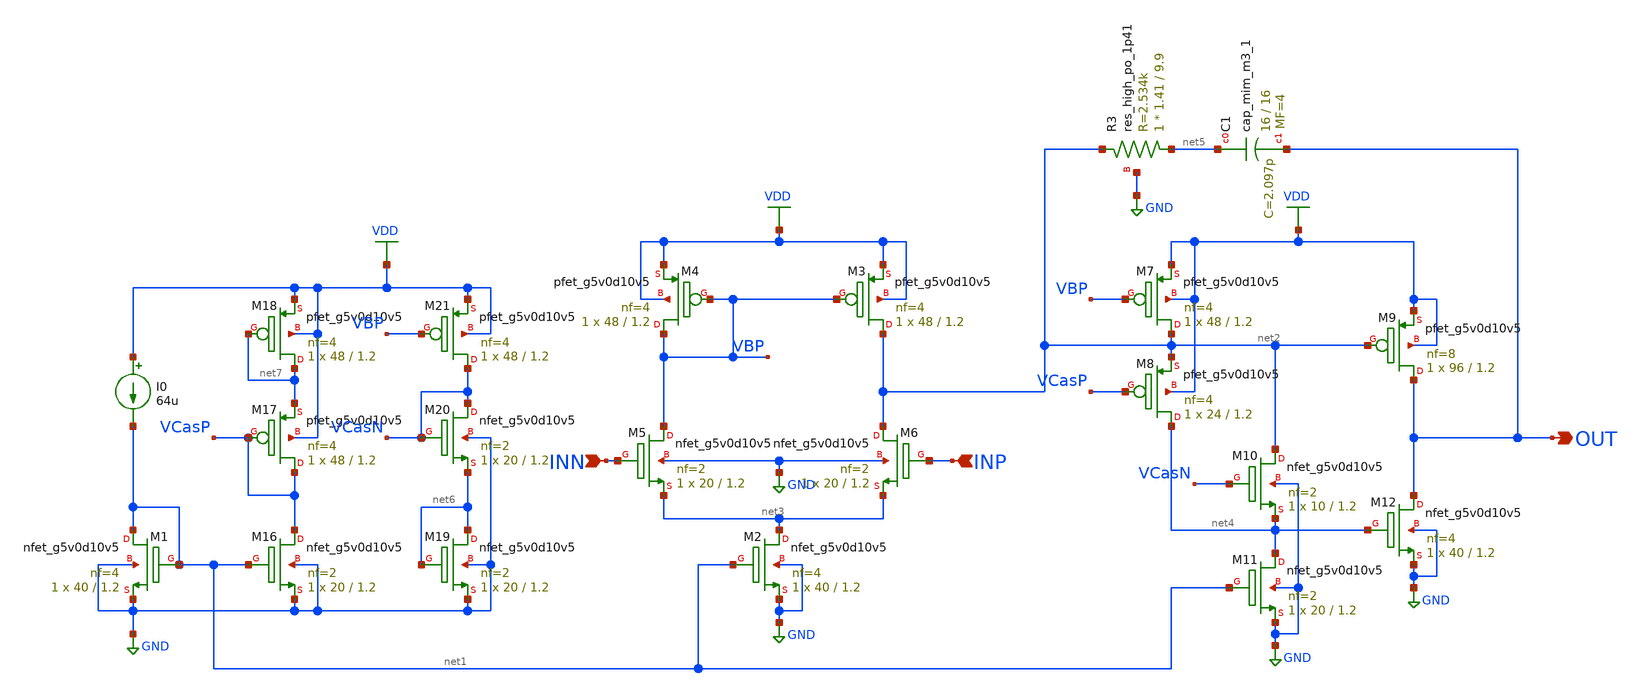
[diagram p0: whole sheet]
** sch_path: Amplifier_PushPull.sch
**.subckt Amplifier_PushPull INN OUT INP
*.ipin INN
*.opin OUT
*.ipin INP
XM1 net1 net1 GND GND sky130_fd_pr__nfet_g5v0d10v5 L=1.2 W=40 nf=4 ad='int((nf+1)/2) * W/nf * 0.29' as='int((nf+2)/2) * W/nf * 0.29'
+ pd='2*int((nf+1)/2) * (W/nf + 0.29)' ps='2*int((nf+2)/2) * (W/nf + 0.29)' nrd='0.29 / W' nrs='0.29 / W'
+ sa=0 sb=0 sd=0 mult=1 m=1
I0 VDD net1 64u
XM4 VBP VBP VDD VDD sky130_fd_pr__pfet_g5v0d10v5 L=1.2 W=48 nf=4 ad='int((nf+1)/2) * W/nf * 0.29' as='int((nf+2)/2) * W/nf * 0.29'
+ pd='2*int((nf+1)/2) * (W/nf + 0.29)' ps='2*int((nf+2)/2) * (W/nf + 0.29)' nrd='0.29 / W' nrs='0.29 / W'
+ sa=0 sb=0 sd=0 mult=1 m=1
XM5 VBP INN net3 GND sky130_fd_pr__nfet_g5v0d10v5 L=1.2 W=20 nf=2 ad='int((nf+1)/2) * W/nf * 0.29' as='int((nf+2)/2) * W/nf * 0.29'
+ pd='2*int((nf+1)/2) * (W/nf + 0.29)' ps='2*int((nf+2)/2) * (W/nf + 0.29)' nrd='0.29 / W' nrs='0.29 / W'
+ sa=0 sb=0 sd=0 mult=1 m=1
XM2 net3 net1 GND GND sky130_fd_pr__nfet_g5v0d10v5 L=1.2 W=40 nf=4 ad='int((nf+1)/2) * W/nf * 0.29' as='int((nf+2)/2) * W/nf * 0.29'
+ pd='2*int((nf+1)/2) * (W/nf + 0.29)' ps='2*int((nf+2)/2) * (W/nf + 0.29)' nrd='0.29 / W' nrs='0.29 / W'
+ sa=0 sb=0 sd=0 mult=1 m=1
XM3 net2 VBP VDD VDD sky130_fd_pr__pfet_g5v0d10v5 L=1.2 W=48 nf=4 ad='int((nf+1)/2) * W/nf * 0.29' as='int((nf+2)/2) * W/nf * 0.29'
+ pd='2*int((nf+1)/2) * (W/nf + 0.29)' ps='2*int((nf+2)/2) * (W/nf + 0.29)' nrd='0.29 / W' nrs='0.29 / W'
+ sa=0 sb=0 sd=0 mult=1 m=1
XM6 net2 INP net3 GND sky130_fd_pr__nfet_g5v0d10v5 L=1.2 W=20 nf=2 ad='int((nf+1)/2) * W/nf * 0.29' as='int((nf+2)/2) * W/nf * 0.29'
+ pd='2*int((nf+1)/2) * (W/nf + 0.29)' ps='2*int((nf+2)/2) * (W/nf + 0.29)' nrd='0.29 / W' nrs='0.29 / W'
+ sa=0 sb=0 sd=0 mult=1 m=1
XM7 net2 VBP VDD VDD sky130_fd_pr__pfet_g5v0d10v5 L=1.2 W=48 nf=4 ad='int((nf+1)/2) * W/nf * 0.29' as='int((nf+2)/2) * W/nf * 0.29'
+ pd='2*int((nf+1)/2) * (W/nf + 0.29)' ps='2*int((nf+2)/2) * (W/nf + 0.29)' nrd='0.29 / W' nrs='0.29 / W'
+ sa=0 sb=0 sd=0 mult=1 m=1
XM8 net4 VCasP net2 VDD sky130_fd_pr__pfet_g5v0d10v5 L=1.2 W=24 nf=4 ad='int((nf+1)/2) * W/nf * 0.29'
+ as='int((nf+2)/2) * W/nf * 0.29' pd='2*int((nf+1)/2) * (W/nf + 0.29)' ps='2*int((nf+2)/2) * (W/nf + 0.29)'
+ nrd='0.29 / W' nrs='0.29 / W' sa=0 sb=0 sd=0 mult=1 m=1
XM9 OUT net2 VDD VDD sky130_fd_pr__pfet_g5v0d10v5 L=1.2 W=96 nf=8 ad='int((nf+1)/2) * W/nf * 0.29' as='int((nf+2)/2) * W/nf * 0.29'
+ pd='2*int((nf+1)/2) * (W/nf + 0.29)' ps='2*int((nf+2)/2) * (W/nf + 0.29)' nrd='0.29 / W' nrs='0.29 / W'
+ sa=0 sb=0 sd=0 mult=1 m=1
XM10 net2 VCasN net4 GND sky130_fd_pr__nfet_g5v0d10v5 L=1.2 W=10 nf=2 ad='int((nf+1)/2) * W/nf * 0.29'
+ as='int((nf+2)/2) * W/nf * 0.29' pd='2*int((nf+1)/2) * (W/nf + 0.29)' ps='2*int((nf+2)/2) * (W/nf + 0.29)'
+ nrd='0.29 / W' nrs='0.29 / W' sa=0 sb=0 sd=0 mult=1 m=1
XM11 net4 net1 GND GND sky130_fd_pr__nfet_g5v0d10v5 L=1.2 W=20 nf=2 ad='int((nf+1)/2) * W/nf * 0.29'
+ as='int((nf+2)/2) * W/nf * 0.29' pd='2*int((nf+1)/2) * (W/nf + 0.29)' ps='2*int((nf+2)/2) * (W/nf + 0.29)'
+ nrd='0.29 / W' nrs='0.29 / W' sa=0 sb=0 sd=0 mult=1 m=1
XM12 OUT net4 GND GND sky130_fd_pr__nfet_g5v0d10v5 L=1.2 W=40 nf=4 ad='int((nf+1)/2) * W/nf * 0.29' as='int((nf+2)/2) * W/nf * 0.29'
+ pd='2*int((nf+1)/2) * (W/nf + 0.29)' ps='2*int((nf+2)/2) * (W/nf + 0.29)' nrd='0.29 / W' nrs='0.29 / W'
+ sa=0 sb=0 sd=0 mult=1 m=1
XR3 net5 net2 GND sky130_fd_pr__res_high_po_1p41 L=9.9 mult=1 m=1
XC1 net5 OUT sky130_fd_pr__cap_mim_m3_1 W=16 L=16 MF=4 m=4
XM16 VCasP net1 GND GND sky130_fd_pr__nfet_g5v0d10v5 L=1.2 W=20 nf=2 ad='int((nf+1)/2) * W/nf * 0.29'
+ as='int((nf+2)/2) * W/nf * 0.29' pd='2*int((nf+1)/2) * (W/nf + 0.29)' ps='2*int((nf+2)/2) * (W/nf + 0.29)'
+ nrd='0.29 / W' nrs='0.29 / W' sa=0 sb=0 sd=0 mult=1 m=1
XM17 VCasP VCasP net7 VDD sky130_fd_pr__pfet_g5v0d10v5 L=1.2 W=48 nf=4 ad='int((nf+1)/2) * W/nf * 0.29'
+ as='int((nf+2)/2) * W/nf * 0.29' pd='2*int((nf+1)/2) * (W/nf + 0.29)' ps='2*int((nf+2)/2) * (W/nf + 0.29)'
+ nrd='0.29 / W' nrs='0.29 / W' sa=0 sb=0 sd=0 mult=1 m=1
XM18 net7 net7 VDD VDD sky130_fd_pr__pfet_g5v0d10v5 L=1.2 W=48 nf=4 ad='int((nf+1)/2) * W/nf * 0.29'
+ as='int((nf+2)/2) * W/nf * 0.29' pd='2*int((nf+1)/2) * (W/nf + 0.29)' ps='2*int((nf+2)/2) * (W/nf + 0.29)'
+ nrd='0.29 / W' nrs='0.29 / W' sa=0 sb=0 sd=0 mult=1 m=1
XM19 net6 net6 GND GND sky130_fd_pr__nfet_g5v0d10v5 L=1.2 W=20 nf=2 ad='int((nf+1)/2) * W/nf * 0.29'
+ as='int((nf+2)/2) * W/nf * 0.29' pd='2*int((nf+1)/2) * (W/nf + 0.29)' ps='2*int((nf+2)/2) * (W/nf + 0.29)'
+ nrd='0.29 / W' nrs='0.29 / W' sa=0 sb=0 sd=0 mult=1 m=1
XM20 VCasN VCasN net6 GND sky130_fd_pr__nfet_g5v0d10v5 L=1.2 W=20 nf=2 ad='int((nf+1)/2) * W/nf * 0.29'
+ as='int((nf+2)/2) * W/nf * 0.29' pd='2*int((nf+1)/2) * (W/nf + 0.29)' ps='2*int((nf+2)/2) * (W/nf + 0.29)'
+ nrd='0.29 / W' nrs='0.29 / W' sa=0 sb=0 sd=0 mult=1 m=1
XM21 VCasN VBP VDD VDD sky130_fd_pr__pfet_g5v0d10v5 L=1.2 W=48 nf=4 ad='int((nf+1)/2) * W/nf * 0.29'
+ as='int((nf+2)/2) * W/nf * 0.29' pd='2*int((nf+1)/2) * (W/nf + 0.29)' ps='2*int((nf+2)/2) * (W/nf + 0.29)'
+ nrd='0.29 / W' nrs='0.29 / W' sa=0 sb=0 sd=0 mult=1 m=1
**.ends
.GLOBAL GND
.GLOBAL VDD
.end
